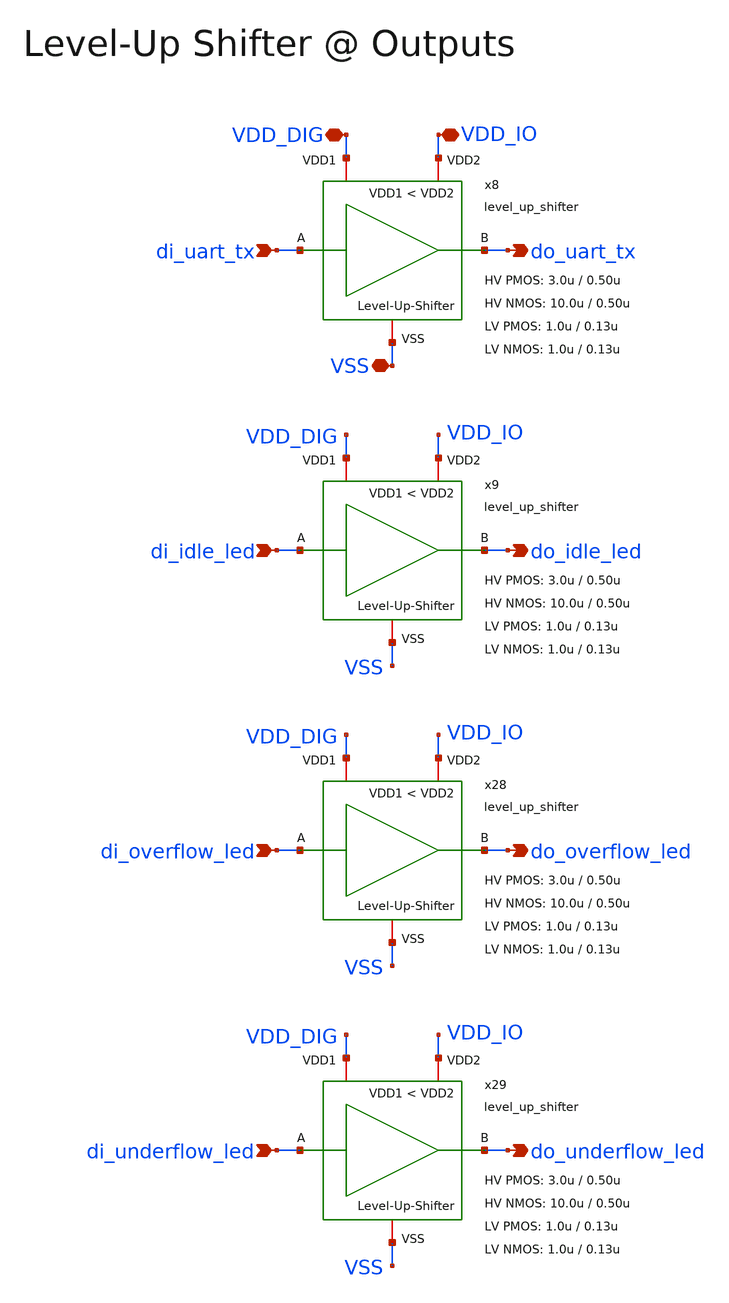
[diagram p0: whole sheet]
** sch_path: SG13G2_ATBS-ADC-main/xschem/top_level/auxiliary/output_hardware.sch
**.subckt output_hardware do_uart_tx do_idle_led do_overflow_led do_underflow_led VSS VDD_IO VDD_DIG
*+ di_idle_led di_overflow_led di_underflow_led di_uart_tx
*.opin do_uart_tx
*.opin do_idle_led
*.opin do_overflow_led
*.opin do_underflow_led
*.iopin VSS
*.iopin VDD_IO
*.iopin VDD_DIG
*.ipin di_idle_led
*.ipin di_overflow_led
*.ipin di_underflow_led
*.ipin di_uart_tx
x8 VDD_IO di_uart_tx do_uart_tx VSS VDD_DIG level_up_shifter W_P_HV=3.0u L_P_HV=0.50u W_N_HV=10.0u
+ L_N_HV=0.50u W_P_LV=1.0u L_P_LV=0.13u W_N_LV=1.0u L_N_LV=0.13u
x9 VDD_IO di_idle_led do_idle_led VSS VDD_DIG level_up_shifter W_P_HV=3.0u L_P_HV=0.50u W_N_HV=10.0u
+ L_N_HV=0.50u W_P_LV=1.0u L_P_LV=0.13u W_N_LV=1.0u L_N_LV=0.13u
x28 VDD_IO di_overflow_led do_overflow_led VSS VDD_DIG level_up_shifter W_P_HV=3.0u L_P_HV=0.50u
+ W_N_HV=10.0u L_N_HV=0.50u W_P_LV=1.0u L_P_LV=0.13u W_N_LV=1.0u L_N_LV=0.13u
x29 VDD_IO di_underflow_led do_underflow_led VSS VDD_DIG level_up_shifter W_P_HV=3.0u L_P_HV=0.50u
+ W_N_HV=10.0u L_N_HV=0.50u W_P_LV=1.0u L_P_LV=0.13u W_N_LV=1.0u L_N_LV=0.13u
**.ends

* expanding   symbol:  level_shifter/level_up_shifter.sym # of pins=5
** sym_path: SG13G2_ATBS-ADC-main/xschem/level_shifter/level_up_shifter.sym
** sch_path: SG13G2_ATBS-ADC-main/xschem/level_shifter/level_up_shifter.sch
.subckt level_up_shifter VDD2 A B VSS VDD1  W_P_HV=3.0u L_P_HV=0.50u W_N_HV=10.0u L_N_HV=0.50u
+ W_P_LV=1.0u L_P_LV=0.13u W_N_LV=1.0u L_N_LV=0.13u
*.ipin A
*.iopin VDD1
*.iopin VSS
*.opin B
*.iopin VDD2
x1 VDD1 A A! VSS inverter_lv W_P=W_P_LV L_P=L_P_LV W_N=W_N_LV L_N=L_N_LV
XM1 net1 A! VSS VSS sg13_hv_nmos w=W_N_HV l=L_N_HV ng=1 m=1 mm_ok=1
XM4 T net1 VDD2 VDD2 sg13_hv_pmos w=W_P_HV l=L_P_HV ng=1 m=1 mm_ok=1
x2 VDD1 A! net2 VSS inverter_lv W_P=W_P_LV L_P=L_P_LV W_N=W_N_LV L_N=L_N_LV
XM3 net1 T VDD2 VDD2 sg13_hv_pmos w=W_P_HV l=L_P_HV ng=1 m=1 mm_ok=1
XM2 T net2 VSS VSS sg13_hv_nmos w=W_N_HV l=L_N_HV ng=1 m=1 mm_ok=1
x3 VDD2 T B VSS inverter_hv W_P=W_P_HV L_P=L_P_HV W_N=0.1*W_N_HV L_N=L_N_HV
.ends


* expanding   symbol:  inverter/inverter_lv.sym # of pins=4
** sym_path: SG13G2_ATBS-ADC-main/xschem/inverter/inverter_lv.sym
** sch_path: SG13G2_ATBS-ADC-main/xschem/inverter/inverter_lv.sch
.subckt inverter_lv VDD vin vout VSS  W_P=3.0u L_P=0.13u W_N=1.0u L_N=0.13u
*.ipin vin
*.iopin VDD
*.iopin VSS
*.opin vout
XM1 vout vin VDD VDD sg13_lv_pmos w=W_P l=L_P ng=1 m=1 mm_ok=1
XM2 vout vin VSS VSS sg13_lv_nmos w=W_N l=L_N ng=1 m=1 mm_ok=1
.ends


* expanding   symbol:  inverter/inverter_hv.sym # of pins=4
** sym_path: SG13G2_ATBS-ADC-main/xschem/inverter/inverter_hv.sym
** sch_path: SG13G2_ATBS-ADC-main/xschem/inverter/inverter_hv.sch
.subckt inverter_hv VDD vin vout VSS  W_P=3.0u L_P=0.50u W_N=1.0u L_N=0.50u
*.ipin vin
*.iopin VDD
*.iopin VSS
*.opin vout
XM1 vout vin VDD VDD sg13_hv_pmos w=W_P l=L_P ng=1 m=1 mm_ok=1
XM2 vout vin VSS VSS sg13_hv_nmos w=W_N l=L_N ng=1 m=1 mm_ok=1
.ends

.end
